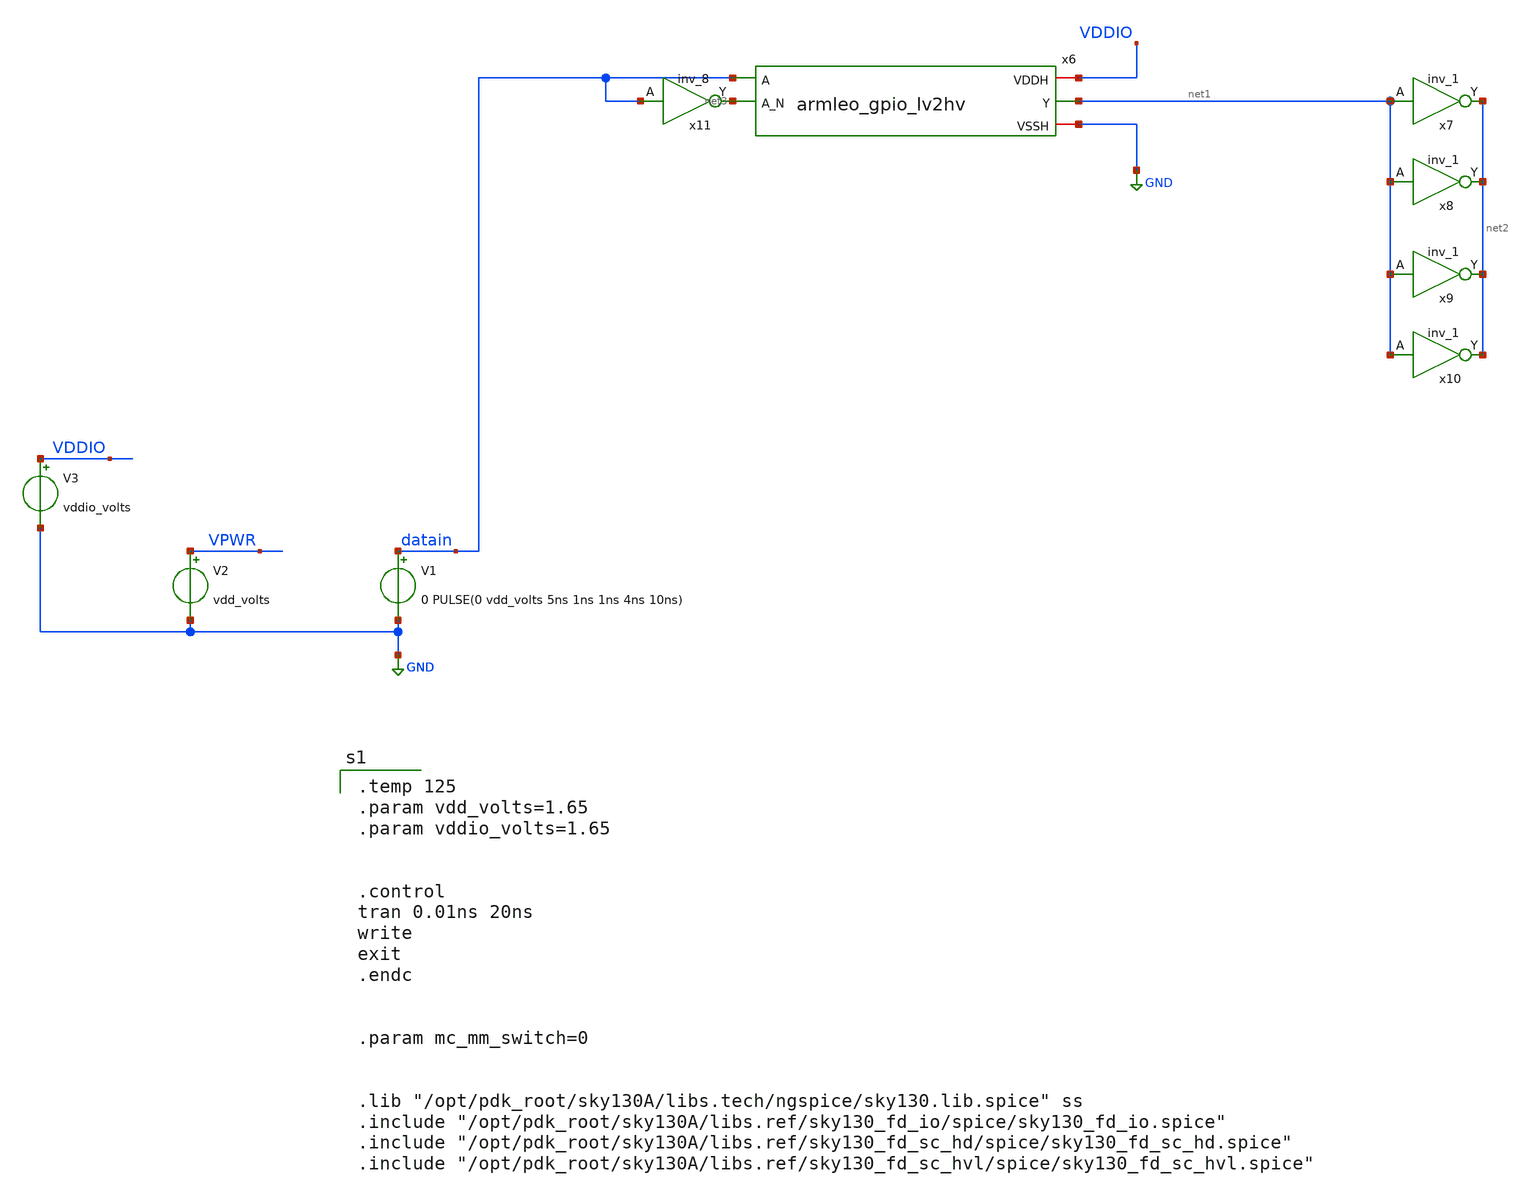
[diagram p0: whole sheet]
** sch_path: xschem/gpio/testbenches/armleo_gpio_lv2hv_tb_1v8.sch
**.subckt armleo_gpio_lv2hv_tb_1v8
V1 datain GND 0 PULSE(0 vdd_volts 5ns 1ns 1ns 4ns 10ns)
V2 VPWR GND vdd_volts
V3 VDDIO GND vddio_volts
x6 VDDIO datain net1 net3 GND armleo_gpio_lv2hv
x7 net1 VGND VGND VDDIO VDDIO net2 sky130_fd_sc_hvl__inv_1
x8 net1 VGND VGND VDDIO VDDIO net2 sky130_fd_sc_hvl__inv_1
x9 net1 VGND VGND VDDIO VDDIO net2 sky130_fd_sc_hvl__inv_1
x10 net1 VGND VGND VDDIO VDDIO net2 sky130_fd_sc_hvl__inv_1
x11 datain GND GND VPWR VPWR net3 sky130_fd_sc_hd__inv_8
**** begin user architecture code

.temp 125
.param vdd_volts=1.65
.param vddio_volts=1.65


.control
tran 0.01ns 20ns
write
exit
.endc


.param mc_mm_switch=0


.lib "/opt/pdk_root/sky130A/libs.tech/ngspice/sky130.lib.spice" ss
.include "/opt/pdk_root/sky130A/libs.ref/sky130_fd_io/spice/sky130_fd_io.spice"
.include "/opt/pdk_root/sky130A/libs.ref/sky130_fd_sc_hd/spice/sky130_fd_sc_hd.spice"
.include "/opt/pdk_root/sky130A/libs.ref/sky130_fd_sc_hvl/spice/sky130_fd_sc_hvl.spice"



**** end user architecture code
**.ends

* expanding   symbol:  gpio/armleo_gpio_lv2hv.sym # of pins=5
** sym_path: xschem/gpio/armleo_gpio_lv2hv.sym
** sch_path: xschem/gpio/armleo_gpio_lv2hv.sch
.subckt armleo_gpio_lv2hv VDDH A Y A_N VSSH
*.ipin A
*.iopin VDDH
*.iopin VSSH
*.opin Y
*.ipin A_N
XM2 VSSH A_N Y VSSH sky130_fd_pr__nfet_g5v0d10v5 L=0.5 W=1 nf=1 ad='int((nf+1)/2) * W/nf * 0.29' as='int((nf+2)/2) * W/nf * 0.29'
+ pd='2*int((nf+1)/2) * (W/nf + 0.29)' ps='2*int((nf+2)/2) * (W/nf + 0.29)' nrd='0.29 / W' nrs='0.29 / W'
+ sa=0 sb=0 sd=0 mult=1 m=1
XM5 N1 A VSSH VSSH sky130_fd_pr__nfet_g5v0d10v5 L=0.5 W=1 nf=1 ad='int((nf+1)/2) * W/nf * 0.29' as='int((nf+2)/2) * W/nf * 0.29'
+ pd='2*int((nf+1)/2) * (W/nf + 0.29)' ps='2*int((nf+2)/2) * (W/nf + 0.29)' nrd='0.29 / W' nrs='0.29 / W'
+ sa=0 sb=0 sd=0 mult=1 m=1
XM4 VDDH Y N2 VDDH sky130_fd_pr__pfet_g5v0d10v5 L=0.5 W=1 nf=1 ad='int((nf+1)/2) * W/nf * 0.29' as='int((nf+2)/2) * W/nf * 0.29'
+ pd='2*int((nf+1)/2) * (W/nf + 0.29)' ps='2*int((nf+2)/2) * (W/nf + 0.29)' nrd='0.29 / W' nrs='0.29 / W'
+ sa=0 sb=0 sd=0 mult=1 m=1
XM7 net1 N1 VDDH VDDH sky130_fd_pr__pfet_g5v0d10v5 L=0.5 W=1 nf=1 ad='int((nf+1)/2) * W/nf * 0.29' as='int((nf+2)/2) * W/nf * 0.29'
+ pd='2*int((nf+1)/2) * (W/nf + 0.29)' ps='2*int((nf+2)/2) * (W/nf + 0.29)' nrd='0.29 / W' nrs='0.29 / W'
+ sa=0 sb=0 sd=0 mult=1 m=1
XM9 N1 A N2 VDDH sky130_fd_pr__pfet_g5v0d10v5 L=0.5 W=1 nf=1 ad='int((nf+1)/2) * W/nf * 0.29' as='int((nf+2)/2) * W/nf * 0.29'
+ pd='2*int((nf+1)/2) * (W/nf + 0.29)' ps='2*int((nf+2)/2) * (W/nf + 0.29)' nrd='0.29 / W' nrs='0.29 / W'
+ sa=0 sb=0 sd=0 mult=1 m=1
XM11 net1 A_N Y VDDH sky130_fd_pr__pfet_g5v0d10v5 L=0.5 W=1 nf=1 ad='int((nf+1)/2) * W/nf * 0.29' as='int((nf+2)/2) * W/nf * 0.29'
+ pd='2*int((nf+1)/2) * (W/nf + 0.29)' ps='2*int((nf+2)/2) * (W/nf + 0.29)' nrd='0.29 / W' nrs='0.29 / W'
+ sa=0 sb=0 sd=0 mult=1 m=1
.ends

.GLOBAL GND
.end
